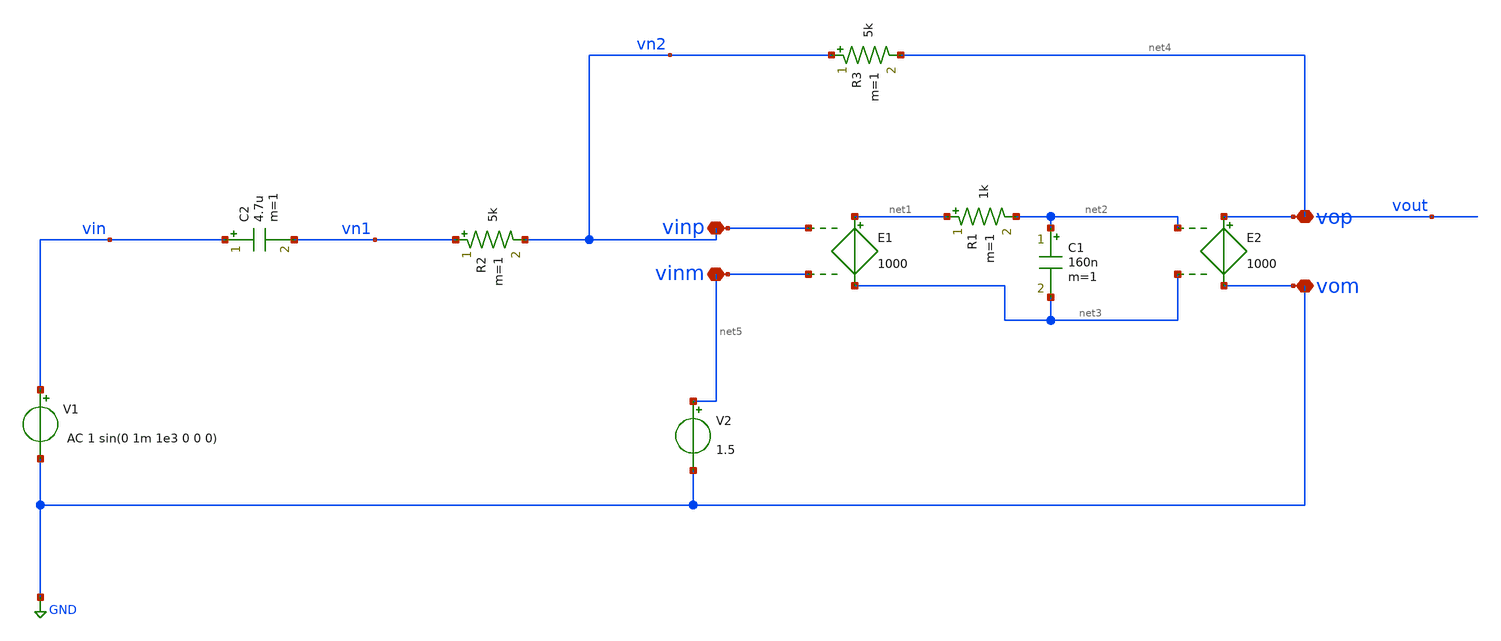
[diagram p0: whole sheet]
** sch_path: xschem/untitled-1.sch
**.subckt untitled-1 vinp vinm vop vom
*.iopin vinp
*.iopin vinm
*.iopin vop
*.iopin vom
E1 net1 net3 vinp vinm 1000
E2 vop vom net2 net3 1000
R1 net1 net2 1k m=1
C1 net2 net3 160n m=1
R2 vn1 vn2 5k m=1
R3 vn2 net4 5k m=1
C2 vin vn1 4.7u m=1
V1 vin GND AC 1 sin(0 1m 1e3 0 0 0)
V2 net5 GND 1.5
**.ends
.GLOBAL GND
.end
